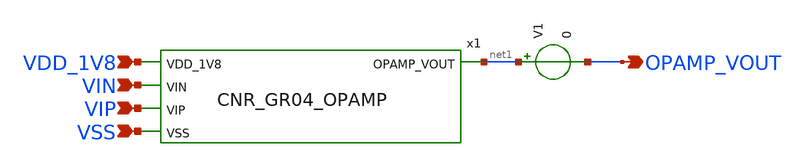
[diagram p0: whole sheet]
** sch_path: design/CNR_GR04_SKY130NM/OPAMP_TEST.sch
**.subckt OPAMP_TEST OPAMP_VOUT VDD_1V8 VIN VIP VSS
*.opin OPAMP_VOUT
*.ipin VDD_1V8
*.ipin VIN
*.ipin VIP
*.ipin VSS
x1 VDD_1V8 net1 VIN VIP VSS CNR_GR04_OPAMP
V1 net1 OPAMP_VOUT 0
**.ends
.end
